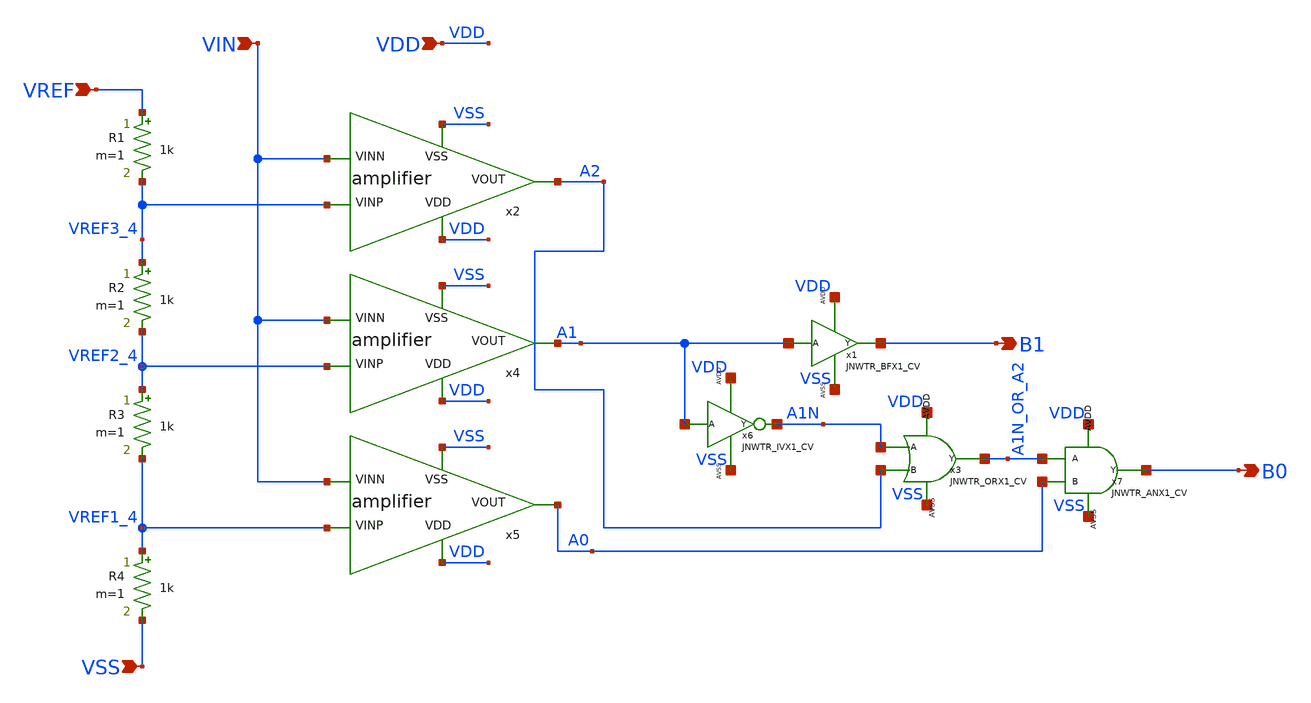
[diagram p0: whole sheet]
** sch_path: design/JNW_GR07_SKY130A/FLASH_ADC_RA.sch
**.subckt FLASH_ADC_RA VDD VSS VIN VREF B1 B0
*.ipin VDD
*.ipin VSS
*.ipin VIN
*.ipin VREF
*.opin B1
*.opin B0
R1 VREF VREF3_4 1k m=1
R2 VREF3_4 VREF2_4 1k m=1
R3 VREF2_4 VREF1_4 1k m=1
R4 VREF1_4 VSS 1k m=1
x2 VDD VREF3_4 VIN A2 VSS amplifier
x4 VDD VREF2_4 VIN A1 VSS amplifier
x5 VDD VREF1_4 VIN A0 VSS amplifier
x3 A1N A2 A1N_OR_A2 VDD VSS JNWTR_ORX1_CV xoffset=0 yoffset=0 angle=0 M=1
x6 A1 A1N VDD VSS JNWTR_IVX1_CV
x7 A1N_OR_A2 A0 B0 VDD VSS JNWTR_ANX1_CV xoffset=0 yoffset=0 angle=0 M=1
**.ends
.end
